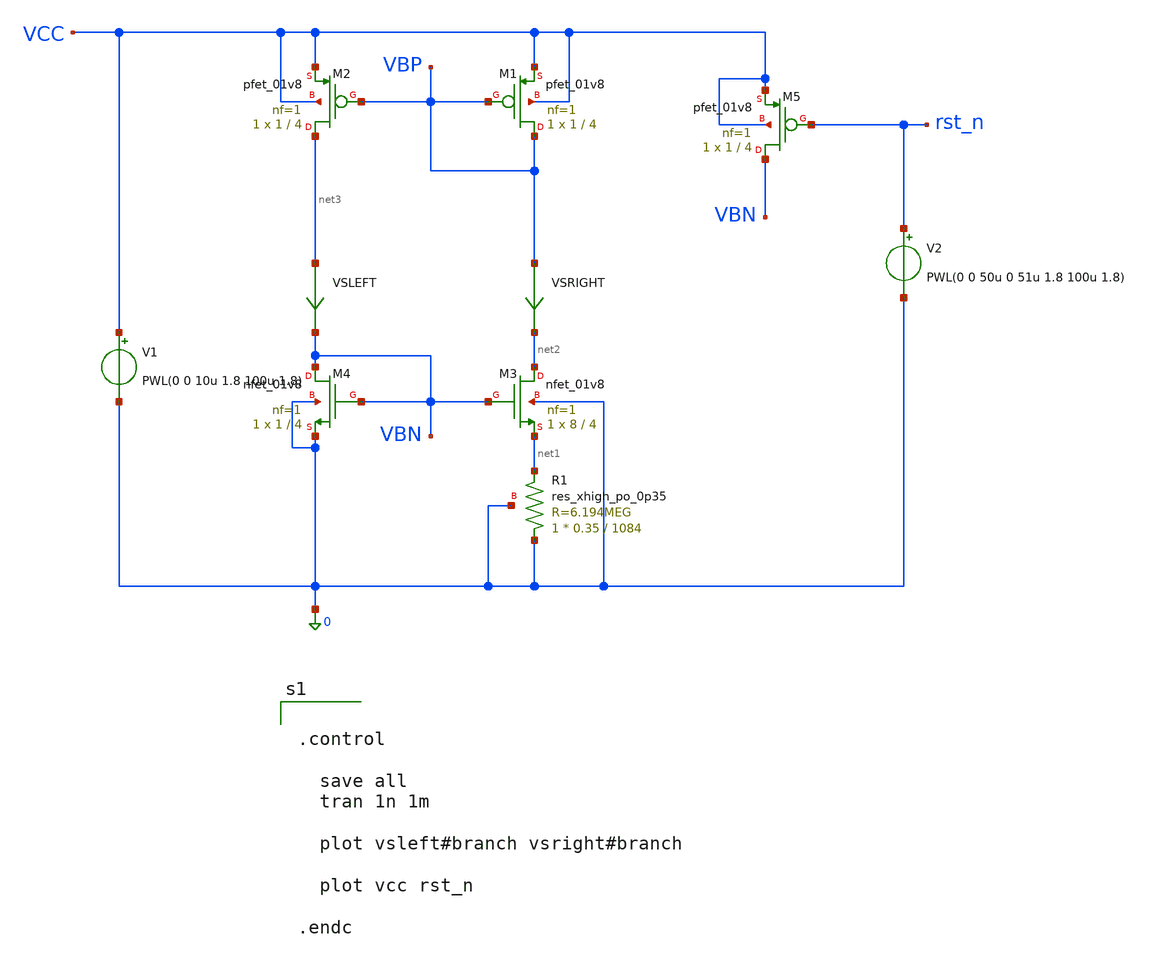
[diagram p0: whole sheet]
** sch_path: schem/bias/bias_bmr_tb.sch
**.subckt bias_bmr_tb
V1 VCC 0 PWL(0 0 10u 1.8 100u 1.8)
XM1 VBP VBP VCC VCC sky130_fd_pr__pfet_01v8 L=4 W=1 nf=1 ad='int((1 + 1)/2) * 1 / 1 * 0.29' as='int((1 + 2)/2) * 1 / 1 * 0.29'
+ pd='2*int((1 + 1)/2) * (1 / 1 + 0.29)' ps='2*int((1 + 2)/2) * (1 / 1 + 0.29)' nrd='0.29 / 1 ' nrs='0.29 / 1 '
+ sa=0 sb=0 sd=0 mult=1 m=1
XM2 net3 VBP VCC VCC sky130_fd_pr__pfet_01v8 L=4 W=1 nf=1 ad='int((1 + 1)/2) * 1 / 1 * 0.29' as='int((1 + 2)/2) * 1 / 1 * 0.29'
+ pd='2*int((1 + 1)/2) * (1 / 1 + 0.29)' ps='2*int((1 + 2)/2) * (1 / 1 + 0.29)' nrd='0.29 / 1 ' nrs='0.29 / 1 '
+ sa=0 sb=0 sd=0 mult=1 m=1
XM3 net2 VBN net1 0 sky130_fd_pr__nfet_01v8 L=4 W=8 nf=1 ad='int((1 + 1)/2) * 8 / 1 * 0.29' as='int((1 + 2)/2) * 8 / 1 * 0.29'
+ pd='2*int((1 + 1)/2) * (8 / 1 + 0.29)' ps='2*int((1 + 2)/2) * (8 / 1 + 0.29)' nrd='0.29 / 8 ' nrs='0.29 / 8 '
+ sa=0 sb=0 sd=0 mult=1 m=1
XM4 VBN VBN 0 0 sky130_fd_pr__nfet_01v8 L=4 W=1 nf=1 ad='int((1 + 1)/2) * 1 / 1 * 0.29' as='int((1 + 2)/2) * 1 / 1 * 0.29'
+ pd='2*int((1 + 1)/2) * (1 / 1 + 0.29)' ps='2*int((1 + 2)/2) * (1 / 1 + 0.29)' nrd='0.29 / 1 ' nrs='0.29 / 1 '
+ sa=0 sb=0 sd=0 mult=1 m=1
XR1 0 net1 0 sky130_fd_pr__res_xhigh_po_0p35 L=1084 mult=1 m=1
VSRIGHT VBP net2 0
.save i(vsright)
VSLEFT net3 VBN 0
.save i(vsleft)
XM5 VBN rst_n VCC VCC sky130_fd_pr__pfet_01v8 L=4 W=1 nf=1 ad='int((1 + 1)/2) * 1 / 1 * 0.29' as='int((1 + 2)/2) * 1 / 1 * 0.29'
+ pd='2*int((1 + 1)/2) * (1 / 1 + 0.29)' ps='2*int((1 + 2)/2) * (1 / 1 + 0.29)' nrd='0.29 / 1 ' nrs='0.29 / 1 '
+ sa=0 sb=0 sd=0 mult=1 m=1
V2 rst_n 0 PWL(0 0 50u 0 51u 1.8 100u 1.8)
**** begin user architecture code

** opencircuitdesign pdks install
.lib $::SKYWATER_MODELS/sky130.lib.spice tt



.control

  save all
  tran 1n 1m

  plot vsleft#branch vsright#branch

  plot vcc rst_n

.endc


**** end user architecture code
**.ends
.end
